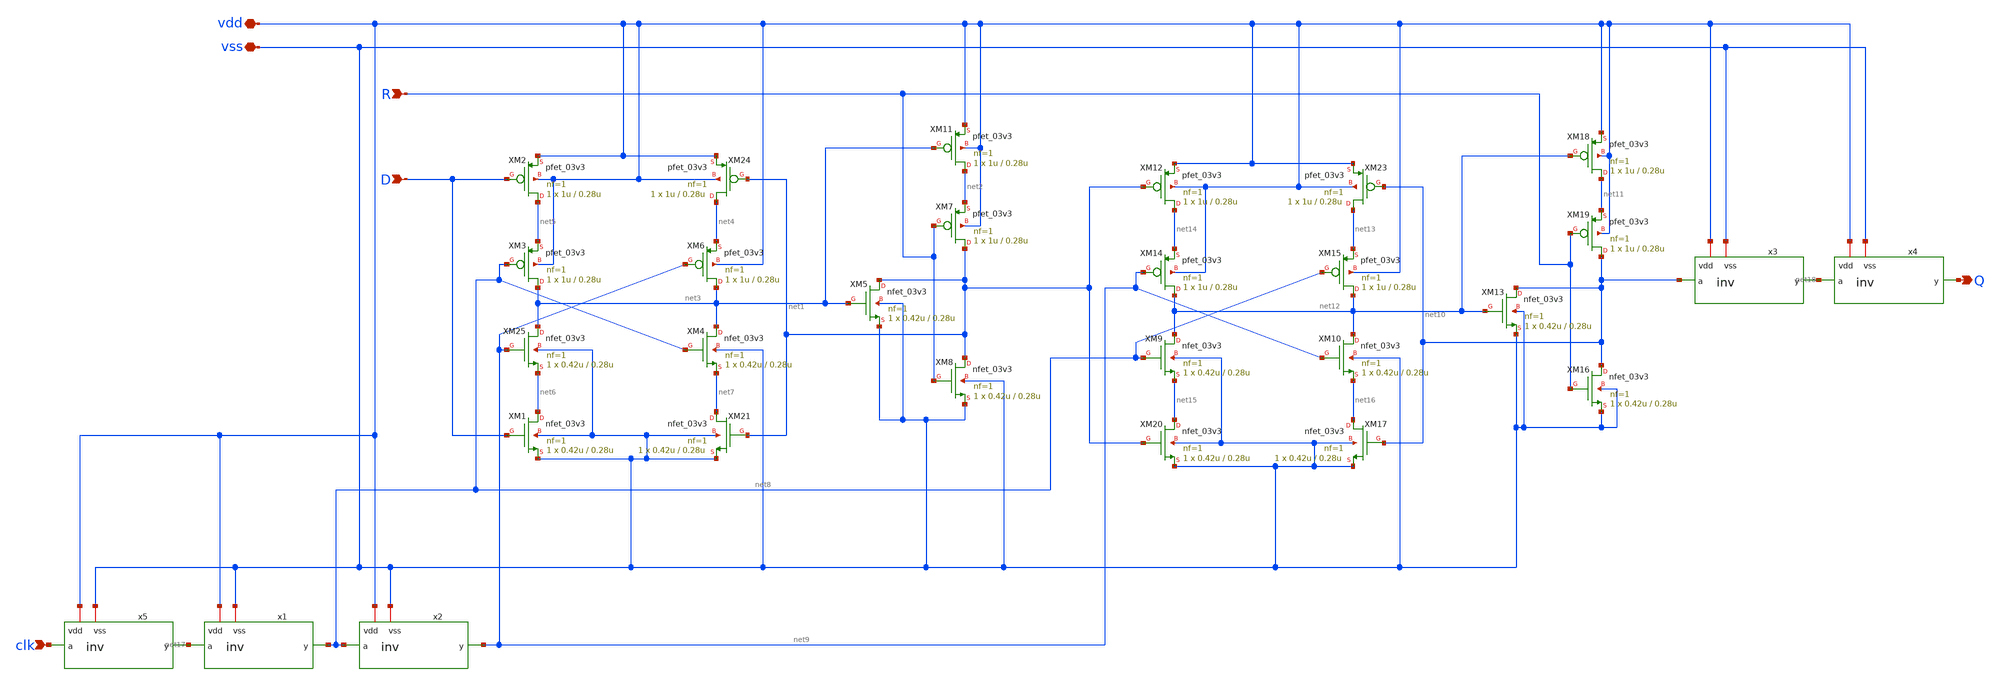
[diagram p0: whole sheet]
** sch_path: member_project/ice458/dynamic_comparator/xschem/rs_ff.sch
**.subckt rs_ff D R Q vdd vss clk
*.ipin D
*.ipin R
*.opin Q
*.iopin vdd
*.iopin vss
*.ipin clk
x1 vdd net17 net8 vss inv
x2 vdd net8 net9 vss inv
x3 vdd net10 net18 vss inv
x4 vdd net18 Q vss inv
x5 vdd clk net17 vss inv
XM25 net3 net9 net6 vss nfet_03v3 L=0.28u W=0.42u nf=1 ad='int((nf+1)/2) * W/nf * 0.18u' as='int((nf+2)/2) * W/nf * 0.18u'
+ pd='2*int((nf+1)/2) * (W/nf + 0.18u)' ps='2*int((nf+2)/2) * (W/nf + 0.18u)' nrd='0.18u / W' nrs='0.18u / W'
+ sa=0 sb=0 sd=0 m=1
XM2 net5 D vdd vdd pfet_03v3 L=0.28u W=1u nf=1 ad='int((nf+1)/2) * W/nf * 0.18u' as='int((nf+2)/2) * W/nf * 0.18u'
+ pd='2*int((nf+1)/2) * (W/nf + 0.18u)' ps='2*int((nf+2)/2) * (W/nf + 0.18u)' nrd='0.18u / W' nrs='0.18u / W'
+ sa=0 sb=0 sd=0 m=1
XM3 net3 net8 net5 vdd pfet_03v3 L=0.28u W=1u nf=1 ad='int((nf+1)/2) * W/nf * 0.18u' as='int((nf+2)/2) * W/nf * 0.18u'
+ pd='2*int((nf+1)/2) * (W/nf + 0.18u)' ps='2*int((nf+2)/2) * (W/nf + 0.18u)' nrd='0.18u / W' nrs='0.18u / W'
+ sa=0 sb=0 sd=0 m=1
XM6 net3 net9 net4 vdd pfet_03v3 L=0.28u W=1u nf=1 ad='int((nf+1)/2) * W/nf * 0.18u' as='int((nf+2)/2) * W/nf * 0.18u'
+ pd='2*int((nf+1)/2) * (W/nf + 0.18u)' ps='2*int((nf+2)/2) * (W/nf + 0.18u)' nrd='0.18u / W' nrs='0.18u / W'
+ sa=0 sb=0 sd=0 m=1
XM7 net1 R net2 vdd pfet_03v3 L=0.28u W=1u nf=1 ad='int((nf+1)/2) * W/nf * 0.18u' as='int((nf+2)/2) * W/nf * 0.18u'
+ pd='2*int((nf+1)/2) * (W/nf + 0.18u)' ps='2*int((nf+2)/2) * (W/nf + 0.18u)' nrd='0.18u / W' nrs='0.18u / W'
+ sa=0 sb=0 sd=0 m=1
XM11 net2 net3 vdd vdd pfet_03v3 L=0.28u W=1u nf=1 ad='int((nf+1)/2) * W/nf * 0.18u' as='int((nf+2)/2) * W/nf * 0.18u'
+ pd='2*int((nf+1)/2) * (W/nf + 0.18u)' ps='2*int((nf+2)/2) * (W/nf + 0.18u)' nrd='0.18u / W' nrs='0.18u / W'
+ sa=0 sb=0 sd=0 m=1
XM12 net14 net1 vdd vdd pfet_03v3 L=0.28u W=1u nf=1 ad='int((nf+1)/2) * W/nf * 0.18u' as='int((nf+2)/2) * W/nf * 0.18u'
+ pd='2*int((nf+1)/2) * (W/nf + 0.18u)' ps='2*int((nf+2)/2) * (W/nf + 0.18u)' nrd='0.18u / W' nrs='0.18u / W'
+ sa=0 sb=0 sd=0 m=1
XM14 net12 net9 net14 vdd pfet_03v3 L=0.28u W=1u nf=1 ad='int((nf+1)/2) * W/nf * 0.18u' as='int((nf+2)/2) * W/nf * 0.18u'
+ pd='2*int((nf+1)/2) * (W/nf + 0.18u)' ps='2*int((nf+2)/2) * (W/nf + 0.18u)' nrd='0.18u / W' nrs='0.18u / W'
+ sa=0 sb=0 sd=0 m=1
XM15 net12 net8 net13 vdd pfet_03v3 L=0.28u W=1u nf=1 ad='int((nf+1)/2) * W/nf * 0.18u' as='int((nf+2)/2) * W/nf * 0.18u'
+ pd='2*int((nf+1)/2) * (W/nf + 0.18u)' ps='2*int((nf+2)/2) * (W/nf + 0.18u)' nrd='0.18u / W' nrs='0.18u / W'
+ sa=0 sb=0 sd=0 m=1
XM18 net11 net12 vdd vdd pfet_03v3 L=0.28u W=1u nf=1 ad='int((nf+1)/2) * W/nf * 0.18u' as='int((nf+2)/2) * W/nf * 0.18u'
+ pd='2*int((nf+1)/2) * (W/nf + 0.18u)' ps='2*int((nf+2)/2) * (W/nf + 0.18u)' nrd='0.18u / W' nrs='0.18u / W'
+ sa=0 sb=0 sd=0 m=1
XM19 net10 R net11 vdd pfet_03v3 L=0.28u W=1u nf=1 ad='int((nf+1)/2) * W/nf * 0.18u' as='int((nf+2)/2) * W/nf * 0.18u'
+ pd='2*int((nf+1)/2) * (W/nf + 0.18u)' ps='2*int((nf+2)/2) * (W/nf + 0.18u)' nrd='0.18u / W' nrs='0.18u / W'
+ sa=0 sb=0 sd=0 m=1
XM23 net13 net10 vdd vdd pfet_03v3 L=0.28u W=1u nf=1 ad='int((nf+1)/2) * W/nf * 0.18u' as='int((nf+2)/2) * W/nf * 0.18u'
+ pd='2*int((nf+1)/2) * (W/nf + 0.18u)' ps='2*int((nf+2)/2) * (W/nf + 0.18u)' nrd='0.18u / W' nrs='0.18u / W'
+ sa=0 sb=0 sd=0 m=1
XM24 net4 net1 vdd vdd pfet_03v3 L=0.28u W=1u nf=1 ad='int((nf+1)/2) * W/nf * 0.18u' as='int((nf+2)/2) * W/nf * 0.18u'
+ pd='2*int((nf+1)/2) * (W/nf + 0.18u)' ps='2*int((nf+2)/2) * (W/nf + 0.18u)' nrd='0.18u / W' nrs='0.18u / W'
+ sa=0 sb=0 sd=0 m=1
XM1 net6 D vss vss nfet_03v3 L=0.28u W=0.42u nf=1 ad='int((nf+1)/2) * W/nf * 0.18u' as='int((nf+2)/2) * W/nf * 0.18u'
+ pd='2*int((nf+1)/2) * (W/nf + 0.18u)' ps='2*int((nf+2)/2) * (W/nf + 0.18u)' nrd='0.18u / W' nrs='0.18u / W'
+ sa=0 sb=0 sd=0 m=1
XM4 net3 net8 net7 vss nfet_03v3 L=0.28u W=0.42u nf=1 ad='int((nf+1)/2) * W/nf * 0.18u' as='int((nf+2)/2) * W/nf * 0.18u'
+ pd='2*int((nf+1)/2) * (W/nf + 0.18u)' ps='2*int((nf+2)/2) * (W/nf + 0.18u)' nrd='0.18u / W' nrs='0.18u / W'
+ sa=0 sb=0 sd=0 m=1
XM5 net1 net3 vss vss nfet_03v3 L=0.28u W=0.42u nf=1 ad='int((nf+1)/2) * W/nf * 0.18u' as='int((nf+2)/2) * W/nf * 0.18u'
+ pd='2*int((nf+1)/2) * (W/nf + 0.18u)' ps='2*int((nf+2)/2) * (W/nf + 0.18u)' nrd='0.18u / W' nrs='0.18u / W'
+ sa=0 sb=0 sd=0 m=1
XM8 net1 R vss vss nfet_03v3 L=0.28u W=0.42u nf=1 ad='int((nf+1)/2) * W/nf * 0.18u' as='int((nf+2)/2) * W/nf * 0.18u'
+ pd='2*int((nf+1)/2) * (W/nf + 0.18u)' ps='2*int((nf+2)/2) * (W/nf + 0.18u)' nrd='0.18u / W' nrs='0.18u / W'
+ sa=0 sb=0 sd=0 m=1
XM9 net12 net8 net15 vss nfet_03v3 L=0.28u W=0.42u nf=1 ad='int((nf+1)/2) * W/nf * 0.18u' as='int((nf+2)/2) * W/nf * 0.18u'
+ pd='2*int((nf+1)/2) * (W/nf + 0.18u)' ps='2*int((nf+2)/2) * (W/nf + 0.18u)' nrd='0.18u / W' nrs='0.18u / W'
+ sa=0 sb=0 sd=0 m=1
XM10 net12 net9 net16 vss nfet_03v3 L=0.28u W=0.42u nf=1 ad='int((nf+1)/2) * W/nf * 0.18u' as='int((nf+2)/2) * W/nf * 0.18u'
+ pd='2*int((nf+1)/2) * (W/nf + 0.18u)' ps='2*int((nf+2)/2) * (W/nf + 0.18u)' nrd='0.18u / W' nrs='0.18u / W'
+ sa=0 sb=0 sd=0 m=1
XM13 net10 net12 vss vss nfet_03v3 L=0.28u W=0.42u nf=1 ad='int((nf+1)/2) * W/nf * 0.18u' as='int((nf+2)/2) * W/nf * 0.18u'
+ pd='2*int((nf+1)/2) * (W/nf + 0.18u)' ps='2*int((nf+2)/2) * (W/nf + 0.18u)' nrd='0.18u / W' nrs='0.18u / W'
+ sa=0 sb=0 sd=0 m=1
XM16 net10 R vss vss nfet_03v3 L=0.28u W=0.42u nf=1 ad='int((nf+1)/2) * W/nf * 0.18u' as='int((nf+2)/2) * W/nf * 0.18u'
+ pd='2*int((nf+1)/2) * (W/nf + 0.18u)' ps='2*int((nf+2)/2) * (W/nf + 0.18u)' nrd='0.18u / W' nrs='0.18u / W'
+ sa=0 sb=0 sd=0 m=1
XM17 net16 net10 vss vss nfet_03v3 L=0.28u W=0.42u nf=1 ad='int((nf+1)/2) * W/nf * 0.18u' as='int((nf+2)/2) * W/nf * 0.18u'
+ pd='2*int((nf+1)/2) * (W/nf + 0.18u)' ps='2*int((nf+2)/2) * (W/nf + 0.18u)' nrd='0.18u / W' nrs='0.18u / W'
+ sa=0 sb=0 sd=0 m=1
XM20 net15 net1 vss vss nfet_03v3 L=0.28u W=0.42u nf=1 ad='int((nf+1)/2) * W/nf * 0.18u' as='int((nf+2)/2) * W/nf * 0.18u'
+ pd='2*int((nf+1)/2) * (W/nf + 0.18u)' ps='2*int((nf+2)/2) * (W/nf + 0.18u)' nrd='0.18u / W' nrs='0.18u / W'
+ sa=0 sb=0 sd=0 m=1
XM21 net7 net1 vss vss nfet_03v3 L=0.28u W=0.42u nf=1 ad='int((nf+1)/2) * W/nf * 0.18u' as='int((nf+2)/2) * W/nf * 0.18u'
+ pd='2*int((nf+1)/2) * (W/nf + 0.18u)' ps='2*int((nf+2)/2) * (W/nf + 0.18u)' nrd='0.18u / W' nrs='0.18u / W'
+ sa=0 sb=0 sd=0 m=1
**.ends

* expanding   symbol:  inv.sym # of pins=4
** sym_path: member_project/ice458/dynamic_comparator/xschem/inv.sym
** sch_path: member_project/ice458/dynamic_comparator/xschem/inv.sch
.subckt inv vdd a y vss
*.iopin vdd
*.iopin vss
*.ipin a
*.opin y
XM1 y a vss vss nfet_03v3 L=0.28u W=0.42u nf=1 ad='int((nf+1)/2) * W/nf * 0.18u' as='int((nf+2)/2) * W/nf * 0.18u'
+ pd='2*int((nf+1)/2) * (W/nf + 0.18u)' ps='2*int((nf+2)/2) * (W/nf + 0.18u)' nrd='0.18u / W' nrs='0.18u / W'
+ sa=0 sb=0 sd=0 m=1
XM2 y a vdd vdd pfet_03v3 L=0.28u W=1u nf=1 ad='int((nf+1)/2) * W/nf * 0.18u' as='int((nf+2)/2) * W/nf * 0.18u'
+ pd='2*int((nf+1)/2) * (W/nf + 0.18u)' ps='2*int((nf+2)/2) * (W/nf + 0.18u)' nrd='0.18u / W' nrs='0.18u / W'
+ sa=0 sb=0 sd=0 m=1
.ends

.end
